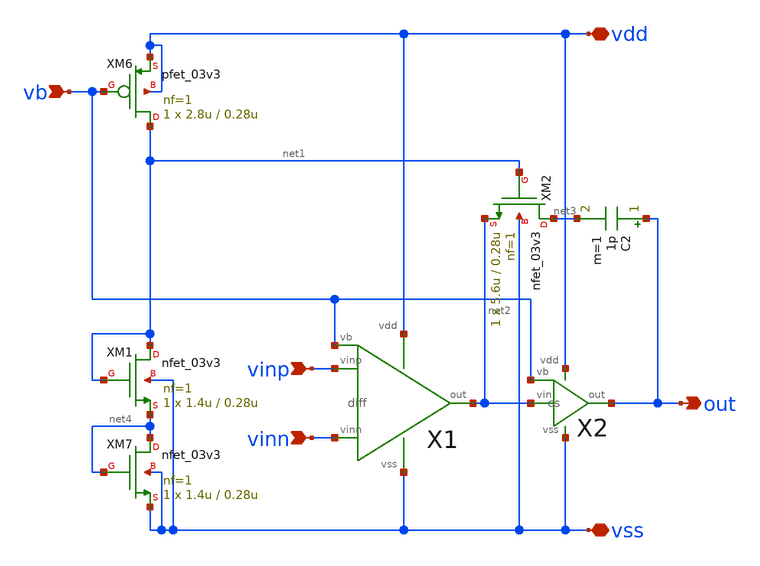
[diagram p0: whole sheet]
** sch_path: opamp/2stage_pc.sch
**.subckt 2stage_pc vinp vinn vb out vdd vss
*.ipin vinp
*.ipin vinn
*.ipin vb
*.opin out
*.iopin vdd
*.iopin vss
X1 vinp vinn net2 vdd vss vb diff
X2 net2 vb out vdd vss cs
C2 out net3 1p m=1
XM6 net1 vb vdd vdd pfet_03v3 L=0.28u W=2.8u nf=1 ad='int((nf+1)/2) * W/nf * 0.18u' as='int((nf+2)/2) * W/nf * 0.18u'
+ pd='2*int((nf+1)/2) * (W/nf + 0.18u)' ps='2*int((nf+2)/2) * (W/nf + 0.18u)' nrd='0.18u / W' nrs='0.18u / W'
+ sa=0 sb=0 sd=0 m=1
XM7 net4 net4 vss vss nfet_03v3 L=0.28u W=1.4u nf=1 ad='int((nf+1)/2) * W/nf * 0.18u' as='int((nf+2)/2) * W/nf * 0.18u'
+ pd='2*int((nf+1)/2) * (W/nf + 0.18u)' ps='2*int((nf+2)/2) * (W/nf + 0.18u)' nrd='0.18u / W' nrs='0.18u / W'
+ sa=0 sb=0 sd=0 m=1
XM1 net1 net1 net4 vss nfet_03v3 L=0.28u W=1.4u nf=1 ad='int((nf+1)/2) * W/nf * 0.18u' as='int((nf+2)/2) * W/nf * 0.18u'
+ pd='2*int((nf+1)/2) * (W/nf + 0.18u)' ps='2*int((nf+2)/2) * (W/nf + 0.18u)' nrd='0.18u / W' nrs='0.18u / W'
+ sa=0 sb=0 sd=0 m=1
XM2 net3 net1 net2 vss nfet_03v3 L=0.28u W=5.6u nf=1 ad='int((nf+1)/2) * W/nf * 0.18u' as='int((nf+2)/2) * W/nf * 0.18u'
+ pd='2*int((nf+1)/2) * (W/nf + 0.18u)' ps='2*int((nf+2)/2) * (W/nf + 0.18u)' nrd='0.18u / W' nrs='0.18u / W'
+ sa=0 sb=0 sd=0 m=1
**.ends
.end
